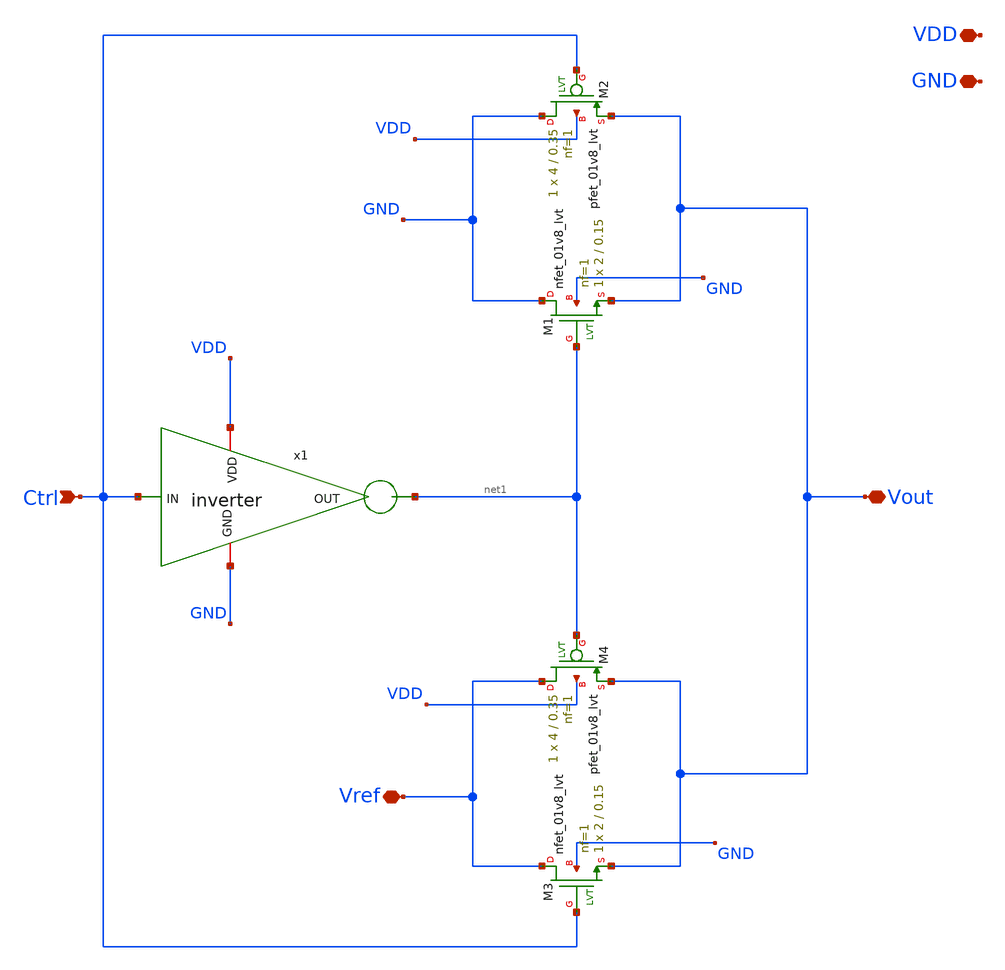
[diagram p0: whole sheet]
** sch_path: 05_mixed_signal/soluzioni/lab01/xschem/T_gate.sch
**.subckt T_gate Ctrl Vout VDD GND Vref
*.ipin Ctrl
*.iopin Vout
*.iopin VDD
*.iopin GND
*.iopin Vref
x1 VDD Ctrl net1 GND inverter
XM1 GND net1 Vout GND sky130_fd_pr__nfet_01v8_lvt L=0.15 W=2 nf=1 ad='int((1 + 1)/2) * 2 / 1 * 0.29'
+ as='int((1 + 2)/2) * 2 / 1 * 0.29' pd='2*int((1 + 1)/2) * (2 / 1 + 0.29)' ps='2*int((1 + 2)/2) * (2 / 1 + 0.29)'
+ nrd='0.29 / 2 ' nrs='0.29 / 2 ' sa=0 sb=0 sd=0 mult=1 m=1
XM2 GND Ctrl Vout VDD sky130_fd_pr__pfet_01v8_lvt L=0.35 W=4 nf=1 ad='int((1 + 1)/2) * 4 / 1 * 0.29'
+ as='int((1 + 2)/2) * 4 / 1 * 0.29' pd='2*int((1 + 1)/2) * (4 / 1 + 0.29)' ps='2*int((1 + 2)/2) * (4 / 1 + 0.29)'
+ nrd='0.29 / 4 ' nrs='0.29 / 4 ' sa=0 sb=0 sd=0 mult=1 m=1
XM3 Vref Ctrl Vout GND sky130_fd_pr__nfet_01v8_lvt L=0.15 W=2 nf=1 ad='int((1 + 1)/2) * 2 / 1 * 0.29'
+ as='int((1 + 2)/2) * 2 / 1 * 0.29' pd='2*int((1 + 1)/2) * (2 / 1 + 0.29)' ps='2*int((1 + 2)/2) * (2 / 1 + 0.29)'
+ nrd='0.29 / 2 ' nrs='0.29 / 2 ' sa=0 sb=0 sd=0 mult=1 m=1
XM4 Vref net1 Vout VDD sky130_fd_pr__pfet_01v8_lvt L=0.35 W=4 nf=1 ad='int((1 + 1)/2) * 4 / 1 * 0.29'
+ as='int((1 + 2)/2) * 4 / 1 * 0.29' pd='2*int((1 + 1)/2) * (4 / 1 + 0.29)' ps='2*int((1 + 2)/2) * (4 / 1 + 0.29)'
+ nrd='0.29 / 4 ' nrs='0.29 / 4 ' sa=0 sb=0 sd=0 mult=1 m=1
**.ends

* expanding   symbol:  inverter.sym # of pins=4
** sym_path: 05_mixed_signal/soluzioni/lab03/xschem/inverter.sym
** sch_path: 05_mixed_signal/soluzioni/lab03/xschem/inverter.sch
.subckt inverter VDD IN OUT GND
*.ipin IN
*.opin OUT
*.iopin VDD
*.iopin GND
XM1 OUT IN GND GND sky130_fd_pr__nfet_01v8_lvt L=0.15 W=2 nf=1 ad='int((1 + 1)/2) * 2 / 1 * 0.29' as='int((1 + 2)/2) * 2 / 1 * 0.29'
+ pd='2*int((1 + 1)/2) * (2 / 1 + 0.29)' ps='2*int((1 + 2)/2) * (2 / 1 + 0.29)' nrd='0.29 / 2 ' nrs='0.29 / 2 '
+ sa=0 sb=0 sd=0 mult=1 m=1
XM2 OUT IN VDD VDD sky130_fd_pr__pfet_01v8_lvt L=0.35 W=4 nf=1 ad='int((1 + 1)/2) * 4 / 1 * 0.29' as='int((1 + 2)/2) * 4 / 1 * 0.29'
+ pd='2*int((1 + 1)/2) * (4 / 1 + 0.29)' ps='2*int((1 + 2)/2) * (4 / 1 + 0.29)' nrd='0.29 / 4 ' nrs='0.29 / 4 '
+ sa=0 sb=0 sd=0 mult=1 m=1
.ends

.end
